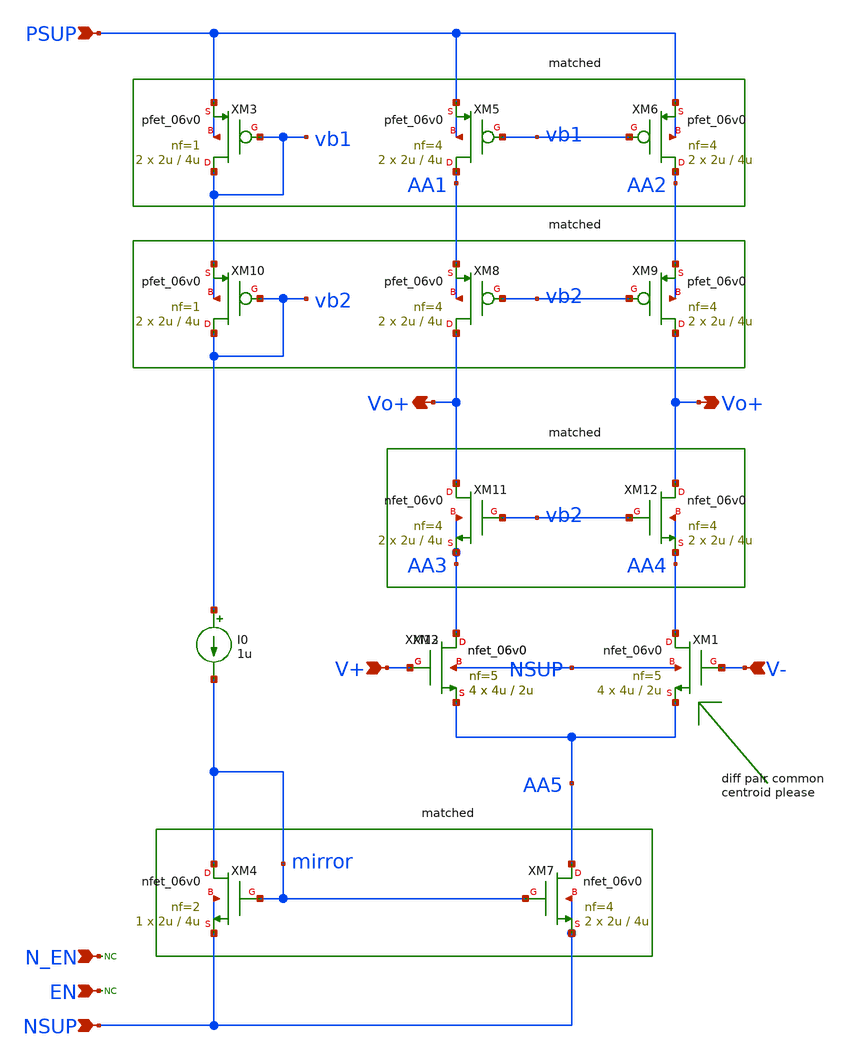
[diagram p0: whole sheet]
** sch_path: xschem/blocks/error_amp/error_amp.sch
**.subckt error_amp PSUP NSUP N_EN EN V+ V- Vo+ Vo+
*.ipin PSUP
*.ipin NSUP
*.ipin N_EN
*.ipin EN
*.ipin V+
*.ipin V-
*.opin Vo+
*.opin Vo+
XM5 AA1 vb1 PSUP PSUP pfet_06v0 L=4u W=2u nf=4 ad='int((nf+1)/2) * W/nf * 0.18u' as='int((nf+2)/2) * W/nf * 0.18u'
+ pd='2*int((nf+1)/2) * (W/nf + 0.18u)' ps='2*int((nf+2)/2) * (W/nf + 0.18u)' nrd='0.18u / W' nrs='0.18u / W'
+ sa=0 sb=0 sd=0 m=2
XM6 AA2 vb1 PSUP PSUP pfet_06v0 L=4u W=2u nf=4 ad='int((nf+1)/2) * W/nf * 0.18u' as='int((nf+2)/2) * W/nf * 0.18u'
+ pd='2*int((nf+1)/2) * (W/nf + 0.18u)' ps='2*int((nf+2)/2) * (W/nf + 0.18u)' nrd='0.18u / W' nrs='0.18u / W'
+ sa=0 sb=0 sd=0 m=2
* noconn N_EN
* noconn EN
XM1 AA4 V- AA5 NSUP nfet_06v0 L=2u W=4u nf=5 ad='int((nf+1)/2) * W/nf * 0.18u' as='int((nf+2)/2) * W/nf * 0.18u'
+ pd='2*int((nf+1)/2) * (W/nf + 0.18u)' ps='2*int((nf+2)/2) * (W/nf + 0.18u)' nrd='0.18u / W' nrs='0.18u / W'
+ sa=0 sb=0 sd=0 m=4
XM2 AA3 V+ AA5 NSUP nfet_06v0 L=2u W=4u nf=5 ad='int((nf+1)/2) * W/nf * 0.18u' as='int((nf+2)/2) * W/nf * 0.18u'
+ pd='2*int((nf+1)/2) * (W/nf + 0.18u)' ps='2*int((nf+2)/2) * (W/nf + 0.18u)' nrd='0.18u / W' nrs='0.18u / W'
+ sa=0 sb=0 sd=0 m=4
XM4 mirror mirror NSUP NSUP nfet_06v0 L=4u W=2u nf=2 ad='int((nf+1)/2) * W/nf * 0.18u' as='int((nf+2)/2) * W/nf * 0.18u'
+ pd='2*int((nf+1)/2) * (W/nf + 0.18u)' ps='2*int((nf+2)/2) * (W/nf + 0.18u)' nrd='0.18u / W' nrs='0.18u / W'
+ sa=0 sb=0 sd=0 m=1
I0 vb2 mirror 1u
XM7 AA5 mirror NSUP NSUP nfet_06v0 L=4u W=2u nf=4 ad='int((nf+1)/2) * W/nf * 0.18u' as='int((nf+2)/2) * W/nf * 0.18u'
+ pd='2*int((nf+1)/2) * (W/nf + 0.18u)' ps='2*int((nf+2)/2) * (W/nf + 0.18u)' nrd='0.18u / W' nrs='0.18u / W'
+ sa=0 sb=0 sd=0 m=2
XM3 vb1 vb1 PSUP PSUP pfet_06v0 L=4u W=2u nf=1 ad='int((nf+1)/2) * W/nf * 0.18u' as='int((nf+2)/2) * W/nf * 0.18u'
+ pd='2*int((nf+1)/2) * (W/nf + 0.18u)' ps='2*int((nf+2)/2) * (W/nf + 0.18u)' nrd='0.18u / W' nrs='0.18u / W'
+ sa=0 sb=0 sd=0 m=2
XM8 Vo+ vb2 AA1 AA1 pfet_06v0 L=4u W=2u nf=4 ad='int((nf+1)/2) * W/nf * 0.18u' as='int((nf+2)/2) * W/nf * 0.18u'
+ pd='2*int((nf+1)/2) * (W/nf + 0.18u)' ps='2*int((nf+2)/2) * (W/nf + 0.18u)' nrd='0.18u / W' nrs='0.18u / W'
+ sa=0 sb=0 sd=0 m=2
XM9 Vo+ vb2 AA2 AA2 pfet_06v0 L=4u W=2u nf=4 ad='int((nf+1)/2) * W/nf * 0.18u' as='int((nf+2)/2) * W/nf * 0.18u'
+ pd='2*int((nf+1)/2) * (W/nf + 0.18u)' ps='2*int((nf+2)/2) * (W/nf + 0.18u)' nrd='0.18u / W' nrs='0.18u / W'
+ sa=0 sb=0 sd=0 m=2
XM10 vb2 vb2 vb1 vb1 pfet_06v0 L=4u W=2u nf=1 ad='int((nf+1)/2) * W/nf * 0.18u' as='int((nf+2)/2) * W/nf * 0.18u'
+ pd='2*int((nf+1)/2) * (W/nf + 0.18u)' ps='2*int((nf+2)/2) * (W/nf + 0.18u)' nrd='0.18u / W' nrs='0.18u / W'
+ sa=0 sb=0 sd=0 m=2
XM13 AA3 V+ AA5 NSUP nfet_06v0 L=2u W=4u nf=5 ad='int((nf+1)/2) * W/nf * 0.18u' as='int((nf+2)/2) * W/nf * 0.18u'
+ pd='2*int((nf+1)/2) * (W/nf + 0.18u)' ps='2*int((nf+2)/2) * (W/nf + 0.18u)' nrd='0.18u / W' nrs='0.18u / W'
+ sa=0 sb=0 sd=0 m=4
XM11 Vo+ vb2 AA3 AA3 nfet_06v0 L=4u W=2u nf=4 ad='int((nf+1)/2) * W/nf * 0.18u' as='int((nf+2)/2) * W/nf * 0.18u'
+ pd='2*int((nf+1)/2) * (W/nf + 0.18u)' ps='2*int((nf+2)/2) * (W/nf + 0.18u)' nrd='0.18u / W' nrs='0.18u / W'
+ sa=0 sb=0 sd=0 m=2
XM12 Vo+ vb2 AA4 AA4 nfet_06v0 L=4u W=2u nf=4 ad='int((nf+1)/2) * W/nf * 0.18u' as='int((nf+2)/2) * W/nf * 0.18u'
+ pd='2*int((nf+1)/2) * (W/nf + 0.18u)' ps='2*int((nf+2)/2) * (W/nf + 0.18u)' nrd='0.18u / W' nrs='0.18u / W'
+ sa=0 sb=0 sd=0 m=2
**.ends
.end
